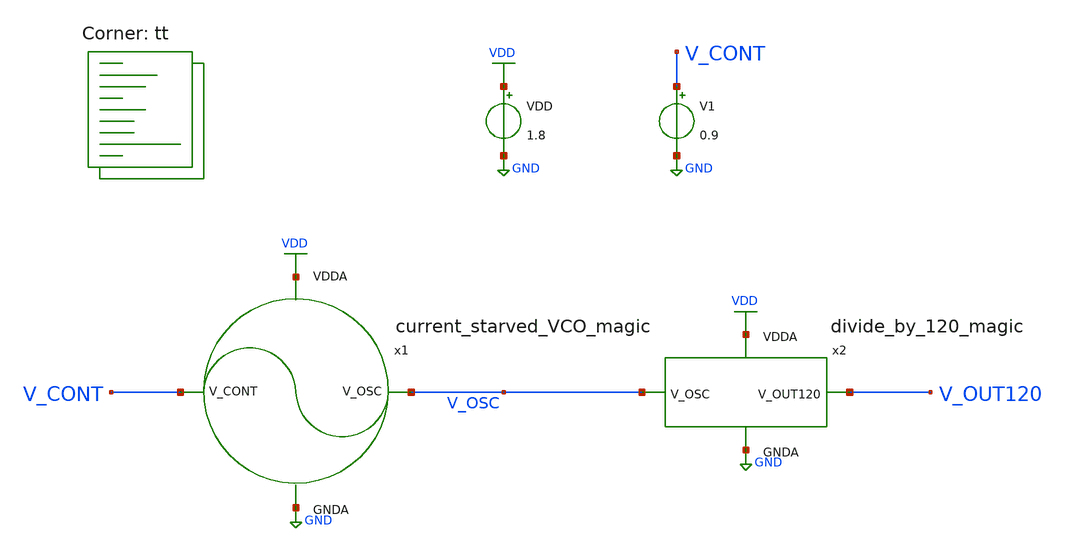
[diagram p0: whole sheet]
** sch_path: projects/pll/divider/magic/divide_by_120/tb_divide_by_120_magic.sch
**.subckt tb_divide_by_120_magic
VDD VDD GND 1.8
V1 V_CONT GND 0.9
x1 VDD V_OSC V_CONT GND current_starved_VCO_magic
x2 VDD V_OUT120 V_OSC GND divide_by_120_magic
**** begin user architecture code



.include /foss/designs/my_design/projects/pll/divider/magic/

.option method=gear
.option wnflag=1

.control

  let v_cont_start = 0.0
  let v_cont_stop = 1.9

  dowhile v_cont_start <= v_cont_stop
    alter v1 $&v_cont_start

    * save all  p(x1:power) p(x2:power)
    * save v(v_osc)
    save v(v_cont) v(v_osc) v(x2.v_out2) v(x2.v_out4) v(x2.v_out8) v(x2.v_out24) v(v_out120)

    * tran 5ps 120ns
    tran 2ps 120ns

    remzerovec

    write tb_divide_by_120_8_{$&v_cont_start}.raw
    * write tb_divide_by_120_8.raw

    * linearize v(v_osc)
    linearize v(v_cont) v(v_osc) v(x2.v_out2) v(x2.v_out4) v(x2.v_out8) v(x2.v_out24) v(v_out120)

    let filename = v_cont_start * 100

    wrdata /foss/designs/my_design/projects/pll/divider/xschem_ngspice/divide_by_120/tb_divide_by_120_8_{$&filename}.txt
+ v(v_osc)
    * wrdata
+ /foss/designs/my_design/projects/pll/divider/xschem_ngspice/divide_by_120/tb_divide_by_120_8_.txt v(v_osc)

    set appendwrite

    reset
    let v_cont_start = v_cont_start + 0.1
   end

.endc



.lib $::SKYWATER_MODELS/sky130.lib.spice tt
**** end user architecture code
**.ends
.GLOBAL GND
.GLOBAL VDD
.end
